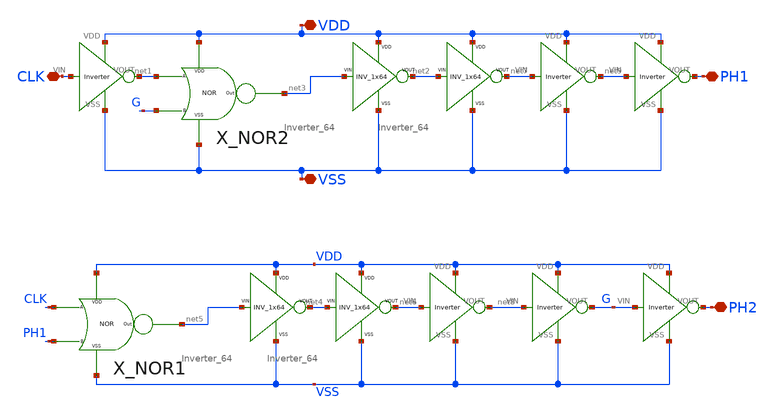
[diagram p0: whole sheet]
** sch_path: xschem/DC_DC_Converter_xschem/OTHERS/DC_DC_Converter_JV9/Non_Overlap_Clk/Non_over_clk.sch
**.subckt Non_over_clk VDD VSS CLK PH1 PH2
*.iopin VDD
*.iopin VSS
*.iopin CLK
*.iopin PH1
*.iopin PH2
X11 VSS VDD CLK net1 Inverter
X1 VSS VDD net7 net9 Inverter
X2 VSS VDD net9 PH1 Inverter
X3 VSS VDD net6 net8 Inverter
X8 VSS VDD net8 G Inverter
X9 VSS VDD G PH2 Inverter
X10 VSS VDD net3 net2 Inverter_64
X4 VSS VDD net2 net7 Inverter_64
X5 VSS VDD net4 net6 Inverter_64
X6 VSS VDD net5 net4 Inverter_64
X_NOR1 VDD VSS CLK PH1 net5 NOR
X_NOR2 VDD VSS net1 G net3 NOR
**.ends
.end
